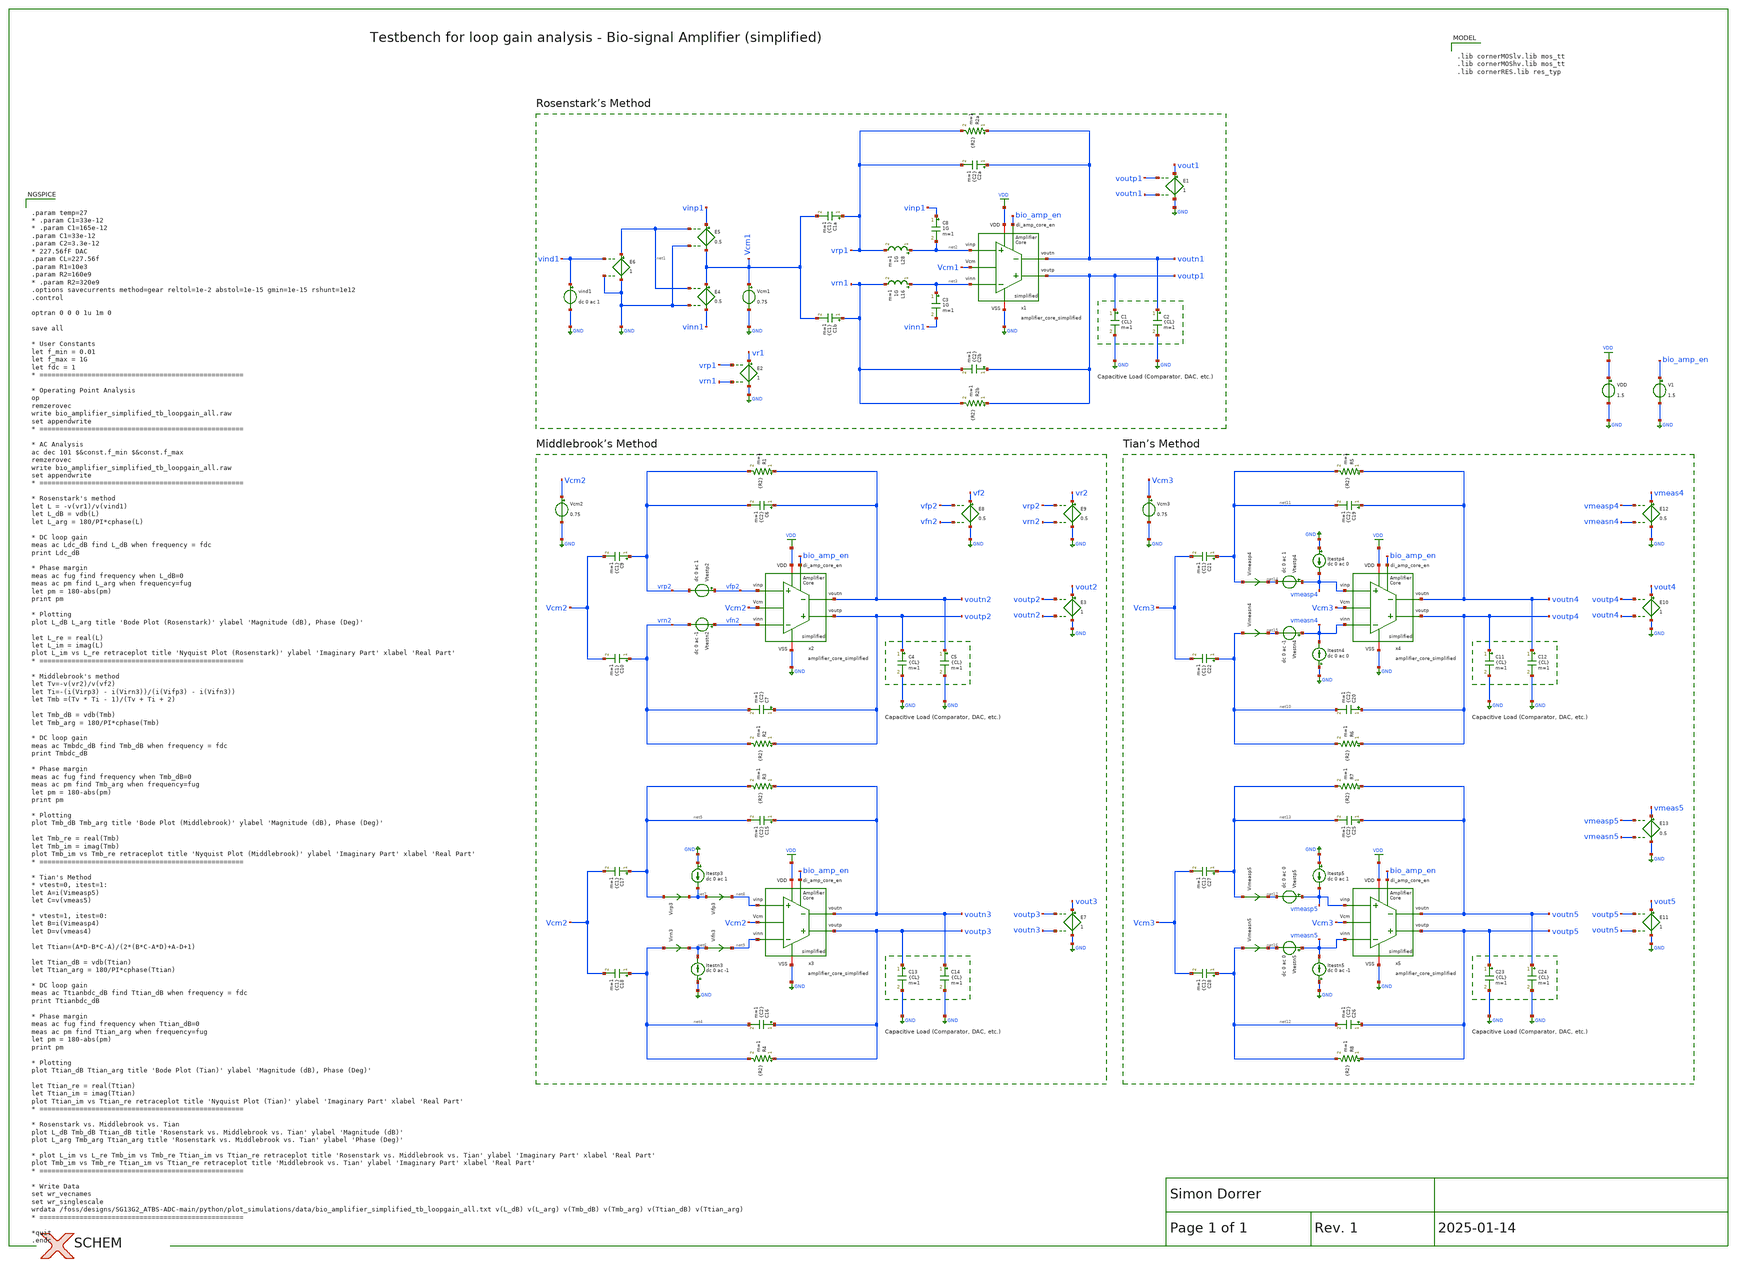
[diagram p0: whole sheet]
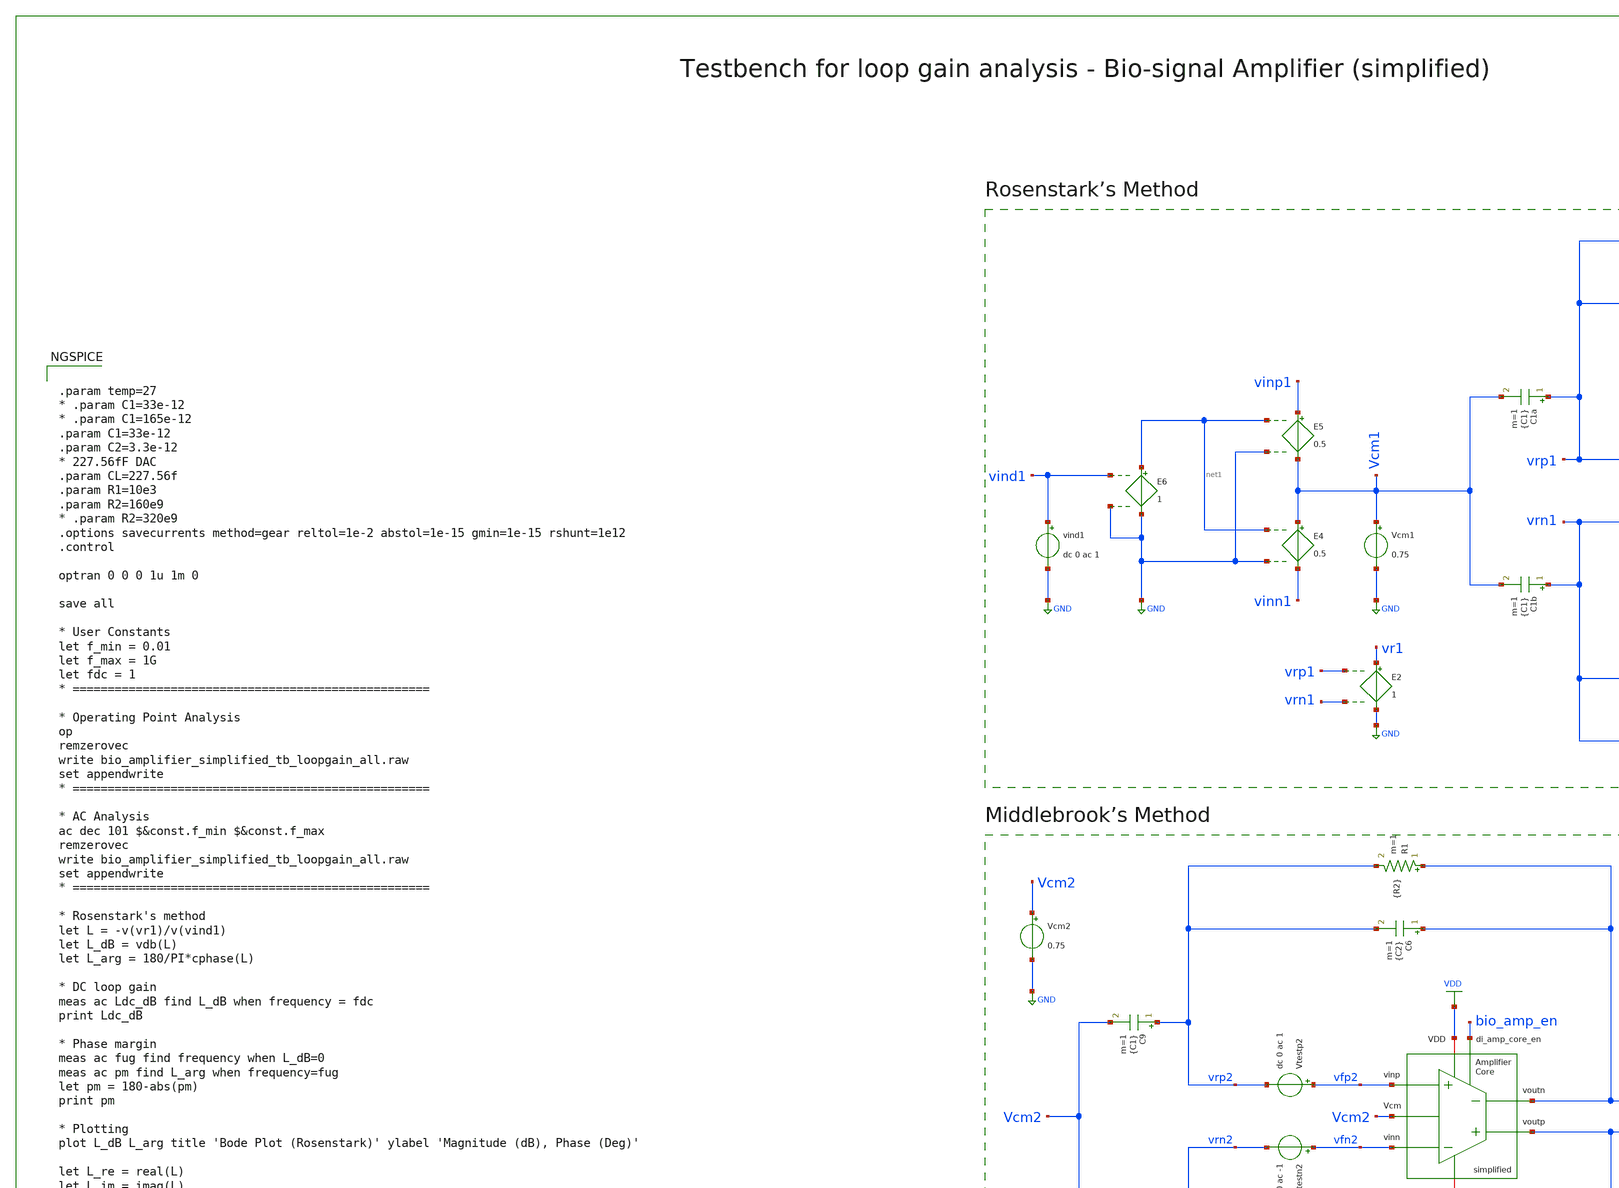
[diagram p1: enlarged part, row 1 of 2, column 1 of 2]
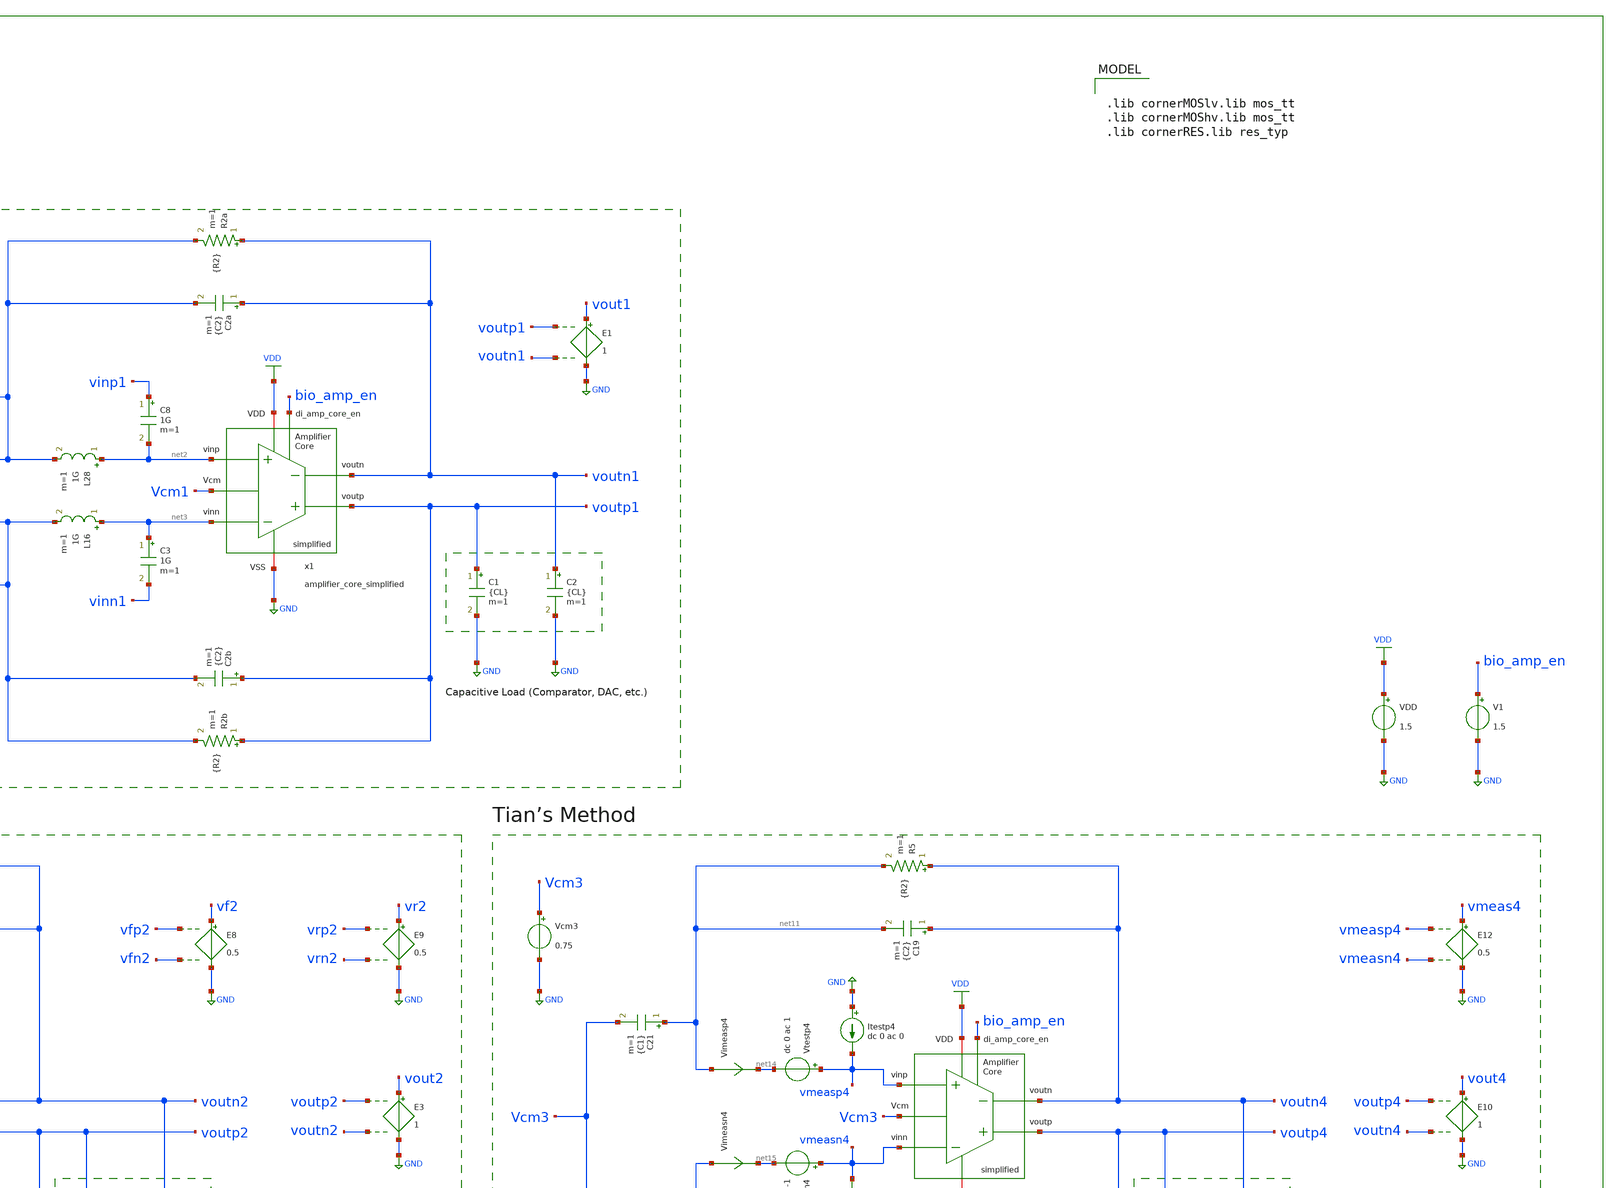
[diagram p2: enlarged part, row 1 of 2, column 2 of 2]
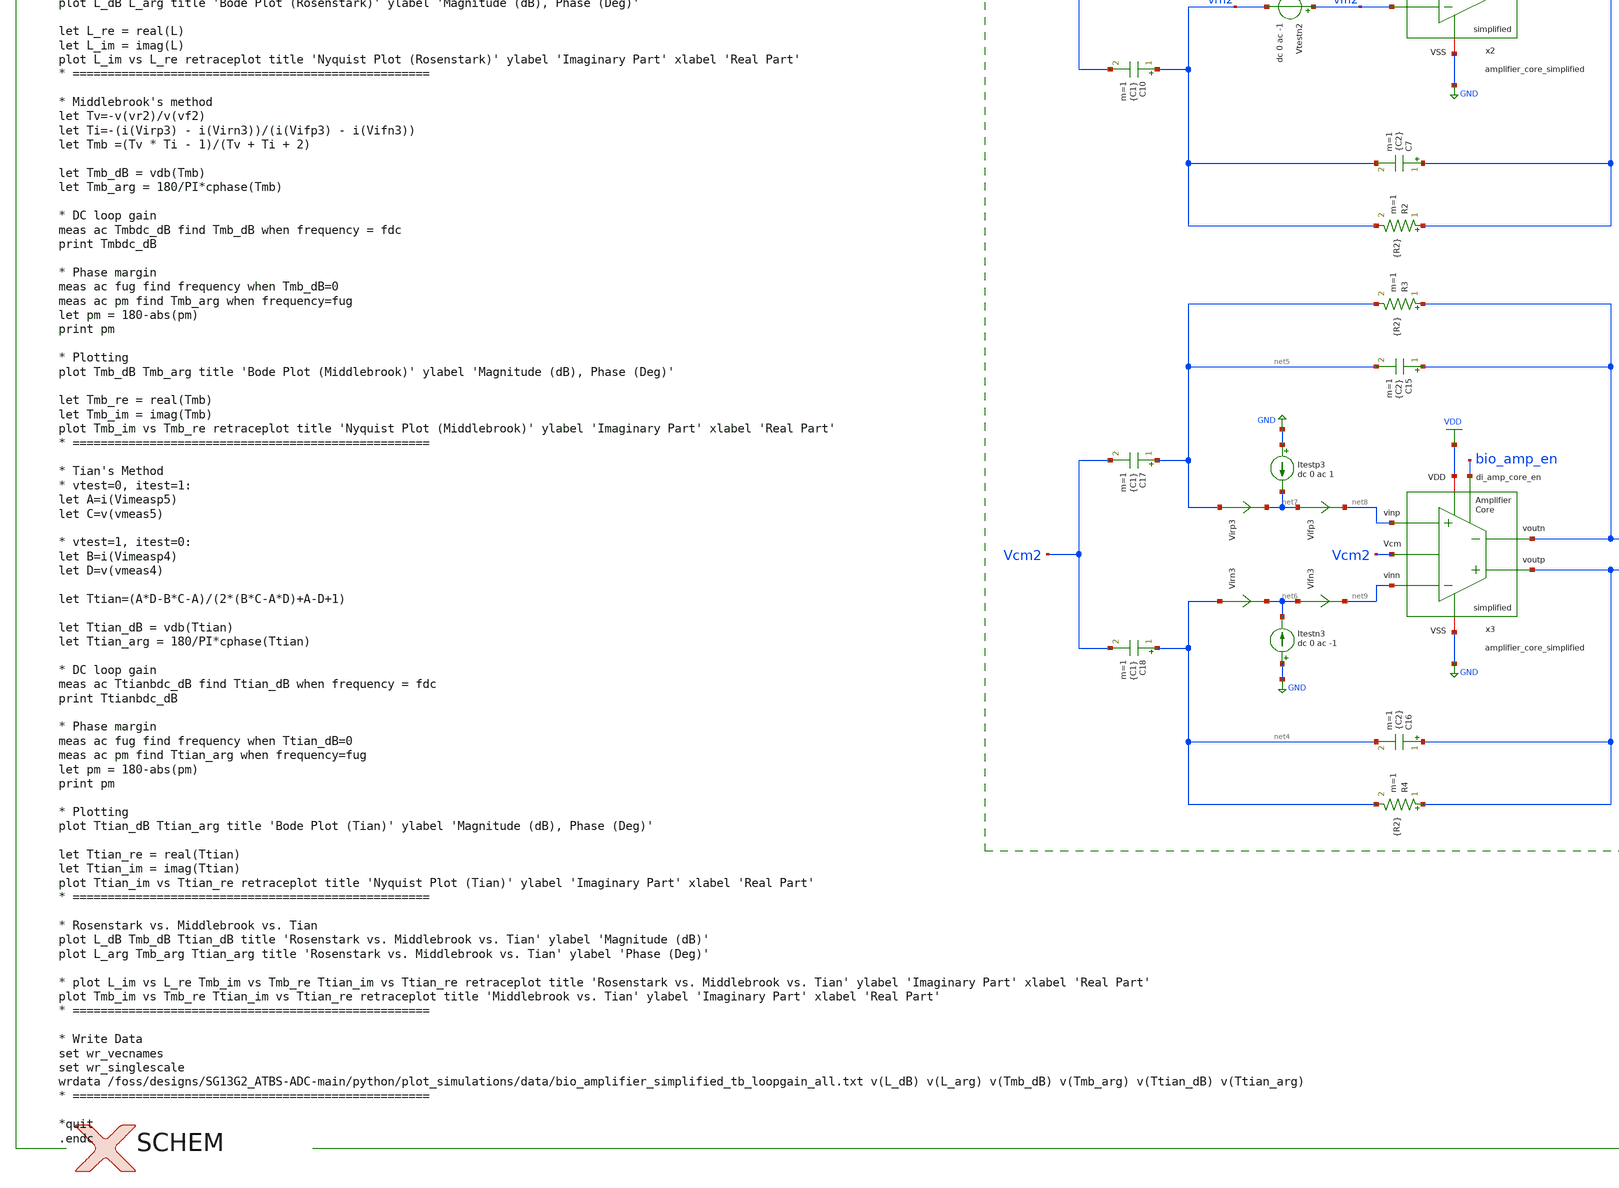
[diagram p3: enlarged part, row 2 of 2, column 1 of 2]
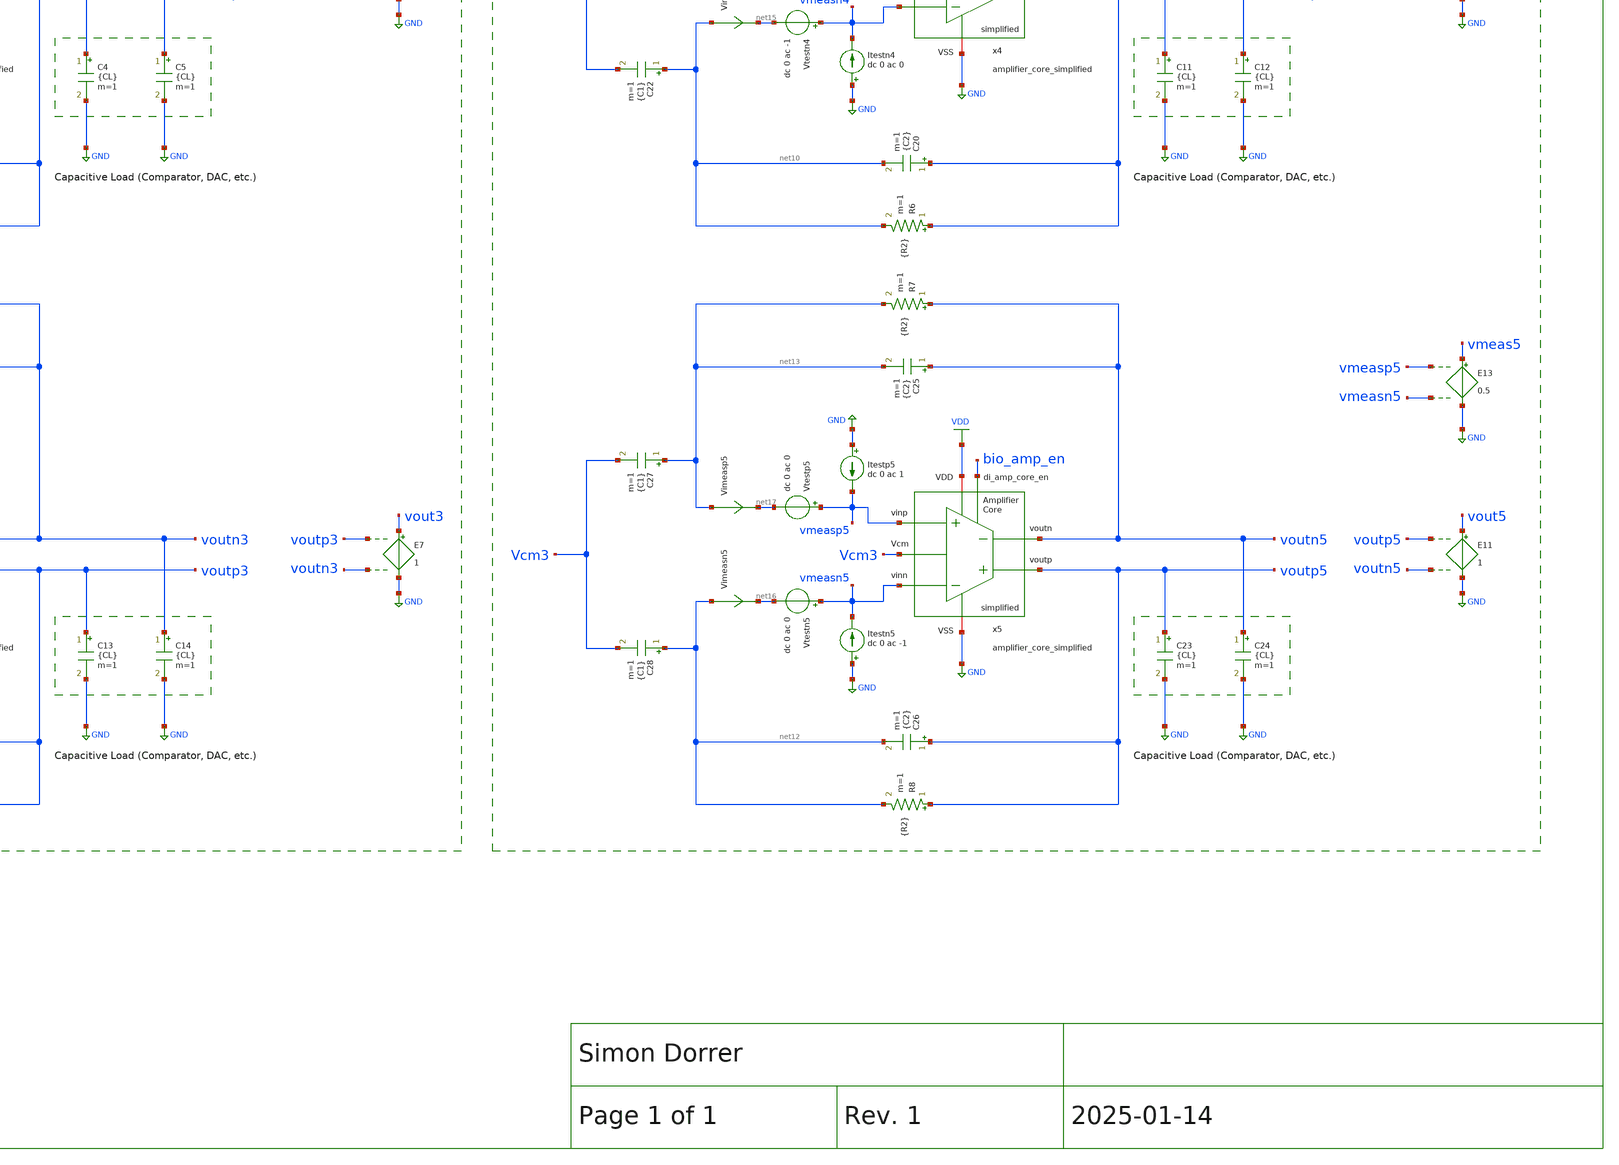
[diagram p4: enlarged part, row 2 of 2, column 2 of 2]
** sch_path: SG13G2_ATBS-ADC-main/xschem/bio_amplifier/testbenches/bio_amplifier_simplified_tb_loopgain_all.sch
**.subckt bio_amplifier_simplified_tb_loopgain_all
VDD VDD GND 1.5
C1 voutp1 GND {CL} m=1
C2 voutn1 GND {CL} m=1
Vcm1 Vcm1 GND 0.75
E4 Vcm1 vinn1 net1 GND 0.5
E5 vinp1 Vcm1 net1 GND 0.5
E6 net1 GND vind1 GND 1
V1 bio_amp_en GND 1.5
E1 vout1 GND voutp1 voutn1 1
vind1 vind1 GND dc 0 ac 1
R2a voutn1 vrp1 {R2} m=1
R2b voutp1 vrn1 {R2} m=1
x1 voutp1 voutn1 bio_amp_en net3 net2 VDD GND Vcm1 amplifier_core_simplified
C2a voutn1 vrp1 {C2} m=1
C2b voutp1 vrn1 {C2} m=1
C1a vrp1 Vcm1 {C1} m=1
C1b vrn1 Vcm1 {C1} m=1
C8 vinp1 net2 1G m=1
L28 net2 vrp1 1G m=1
L16 net3 vrn1 1G m=1
C3 net3 vinn1 1G m=1
E2 vr1 GND vrp1 vrn1 1
C4 voutp2 GND {CL} m=1
C5 voutn2 GND {CL} m=1
E3 vout2 GND voutp2 voutn2 1
R1 voutn2 vrp2 {R2} m=1
R2 voutp2 vrn2 {R2} m=1
x2 voutp2 voutn2 bio_amp_en vfn2 vfp2 VDD GND Vcm2 amplifier_core_simplified
C6 voutn2 vrp2 {C2} m=1
C7 voutp2 vrn2 {C2} m=1
C9 vrp2 Vcm2 {C1} m=1
C10 vrn2 Vcm2 {C1} m=1
C13 voutp3 GND {CL} m=1
C14 voutn3 GND {CL} m=1
E7 vout3 GND voutp3 voutn3 1
R3 voutn3 net5 {R2} m=1
R4 voutp3 net4 {R2} m=1
x3 voutp3 voutn3 bio_amp_en net9 net8 VDD GND Vcm2 amplifier_core_simplified
C15 voutn3 net5 {C2} m=1
C16 voutp3 net4 {C2} m=1
C17 net5 Vcm2 {C1} m=1
C18 net4 Vcm2 {C1} m=1
E8 vf2 GND vfp2 vfn2 0.5
E9 vr2 GND vrp2 vrn2 0.5
Vtestp2 vfp2 vrp2 dc 0 ac 1
Vtestn2 vfn2 vrn2 dc 0 ac -1
Virp3 net5 net7 0
.save i(virp3)
Vifp3 net7 net8 0
.save i(vifp3)
Itestn3 GND net6 dc 0 ac -1
Virn3 net4 net6 0
.save i(virn3)
Vifn3 net6 net9 0
.save i(vifn3)
Itestp3 GND net7 dc 0 ac 1
C11 voutp4 GND {CL} m=1
C12 voutn4 GND {CL} m=1
E10 vout4 GND voutp4 voutn4 1
R5 voutn4 net11 {R2} m=1
R6 voutp4 net10 {R2} m=1
x4 voutp4 voutn4 bio_amp_en vmeasn4 vmeasp4 VDD GND Vcm3 amplifier_core_simplified
C19 voutn4 net11 {C2} m=1
C20 voutp4 net10 {C2} m=1
C21 net11 Vcm3 {C1} m=1
C22 net10 Vcm3 {C1} m=1
C23 voutp5 GND {CL} m=1
C24 voutn5 GND {CL} m=1
E11 vout5 GND voutp5 voutn5 1
R7 voutn5 net13 {R2} m=1
R8 voutp5 net12 {R2} m=1
x5 voutp5 voutn5 bio_amp_en vmeasn5 vmeasp5 VDD GND Vcm3 amplifier_core_simplified
C25 voutn5 net13 {C2} m=1
C26 voutp5 net12 {C2} m=1
C27 net13 Vcm3 {C1} m=1
C28 net12 Vcm3 {C1} m=1
Vtestp4 vmeasp4 net14 dc 0 ac 1
Vimeasp4 net11 net14 0
.save i(vimeasp4)
Itestp4 GND vmeasp4 dc 0 ac 0
Vimeasn4 net10 net15 0
.save i(vimeasn4)
Vtestn4 vmeasn4 net15 dc 0 ac -1
Itestn4 GND vmeasn4 dc 0 ac 0
Vimeasn5 net12 net16 0
.save i(vimeasn5)
Vtestn5 vmeasn5 net16 dc 0 ac 0
Itestn5 GND vmeasn5 dc 0 ac -1
Vtestp5 vmeasp5 net17 dc 0 ac 0
Vimeasp5 net13 net17 0
.save i(vimeasp5)
Itestp5 GND vmeasp5 dc 0 ac 1
E12 vmeas4 GND vmeasp4 vmeasn4 0.5
E13 vmeas5 GND vmeasp5 vmeasn5 0.5
Vcm2 Vcm2 GND 0.75
Vcm3 Vcm3 GND 0.75
**** begin user architecture code

.lib cornerMOSlv.lib mos_tt
.lib cornerMOShv.lib mos_tt
.lib cornerRES.lib res_typ



.param temp=27
* .param C1=33e-12
* .param C1=165e-12
.param C1=33e-12
.param C2=3.3e-12
* 227.56fF DAC
.param CL=227.56f
.param R1=10e3
.param R2=160e9
* .param R2=320e9
.options savecurrents method=gear reltol=1e-2 abstol=1e-15 gmin=1e-15 rshunt=1e12
.control

optran 0 0 0 1u 1m 0

save all

* User Constants
let f_min = 0.01
let f_max = 1G
let fdc = 1
* ===================================================

* Operating Point Analysis
op
remzerovec
write bio_amplifier_simplified_tb_loopgain_all.raw
set appendwrite
* ===================================================

* AC Analysis
ac dec 101 $&const.f_min $&const.f_max
remzerovec
write bio_amplifier_simplified_tb_loopgain_all.raw
set appendwrite
* ===================================================

* Rosenstark's method
let L = -v(vr1)/v(vind1)
let L_dB = vdb(L)
let L_arg = 180/PI*cphase(L)

* DC loop gain
meas ac Ldc_dB find L_dB when frequency = fdc
print Ldc_dB

* Phase margin
meas ac fug find frequency when L_dB=0
meas ac pm find L_arg when frequency=fug
let pm = 180-abs(pm)
print pm

* Plotting
plot L_dB L_arg title 'Bode Plot (Rosenstark)' ylabel 'Magnitude (dB), Phase (Deg)'

let L_re = real(L)
let L_im = imag(L)
plot L_im vs L_re retraceplot title 'Nyquist Plot (Rosenstark)' ylabel 'Imaginary Part' xlabel 'Real
+ Part'
* ===================================================

* Middlebrook's method
let Tv=-v(vr2)/v(vf2)
let Ti=-(i(Virp3) - i(Virn3))/(i(Vifp3) - i(Vifn3))
let Tmb =(Tv * Ti - 1)/(Tv + Ti + 2)

let Tmb_dB = vdb(Tmb)
let Tmb_arg = 180/PI*cphase(Tmb)

* DC loop gain
meas ac Tmbdc_dB find Tmb_dB when frequency = fdc
print Tmbdc_dB

* Phase margin
meas ac fug find frequency when Tmb_dB=0
meas ac pm find Tmb_arg when frequency=fug
let pm = 180-abs(pm)
print pm

* Plotting
plot Tmb_dB Tmb_arg title 'Bode Plot (Middlebrook)' ylabel 'Magnitude (dB), Phase (Deg)'

let Tmb_re = real(Tmb)
let Tmb_im = imag(Tmb)
plot Tmb_im vs Tmb_re retraceplot title 'Nyquist Plot (Middlebrook)' ylabel 'Imaginary Part' xlabel 'Real Part'
* ===================================================

* Tian's Method
* vtest=0, itest=1:
let A=i(Vimeasp5)
let C=v(vmeas5)

* vtest=1, itest=0:
let B=i(Vimeasp4)
let D=v(vmeas4)

let Ttian=(A*D-B*C-A)/(2*(B*C-A*D)+A-D+1)

let Ttian_dB = vdb(Ttian)
let Ttian_arg = 180/PI*cphase(Ttian)

* DC loop gain
meas ac Ttianbdc_dB find Ttian_dB when frequency = fdc
print Ttianbdc_dB

* Phase margin
meas ac fug find frequency when Ttian_dB=0
meas ac pm find Ttian_arg when frequency=fug
let pm = 180-abs(pm)
print pm

* Plotting
plot Ttian_dB Ttian_arg title 'Bode Plot (Tian)' ylabel 'Magnitude (dB), Phase (Deg)'

let Ttian_re = real(Ttian)
let Ttian_im = imag(Ttian)
plot Ttian_im vs Ttian_re retraceplot title 'Nyquist Plot (Tian)' ylabel 'Imaginary Part' xlabel 'Real
+ Part'
* ===================================================

* Rosenstark vs. Middlebrook vs. Tian
plot L_dB Tmb_dB Ttian_dB title 'Rosenstark vs. Middlebrook vs. Tian' ylabel 'Magnitude (dB)'
plot L_arg Tmb_arg Ttian_arg title 'Rosenstark vs. Middlebrook vs. Tian' ylabel 'Phase (Deg)'

* plot L_im vs L_re Tmb_im vs Tmb_re Ttian_im vs Ttian_re retraceplot title 'Rosenstark vs. Middlebrook
*+ vs. Tian' ylabel 'Imaginary Part' xlabel 'Real Part'
plot Tmb_im vs Tmb_re Ttian_im vs Ttian_re retraceplot title 'Middlebrook vs. Tian' ylabel 'Imaginary
+ Part' xlabel 'Real Part'
* ===================================================

* Write Data
set wr_vecnames
set wr_singlescale
wrdata /foss/designs/SG13G2_ATBS-ADC-main/python/plot_simulations/data/bio_amplifier_simplified_tb_loopgain_all.txt v(L_dB) v(L_arg) v(Tmb_dB) v(Tmb_arg) v(Ttian_dB) v(Ttian_arg)
* ===================================================

*quit
.endc


**** end user architecture code
**.ends
.GLOBAL GND
.GLOBAL VDD
.end
